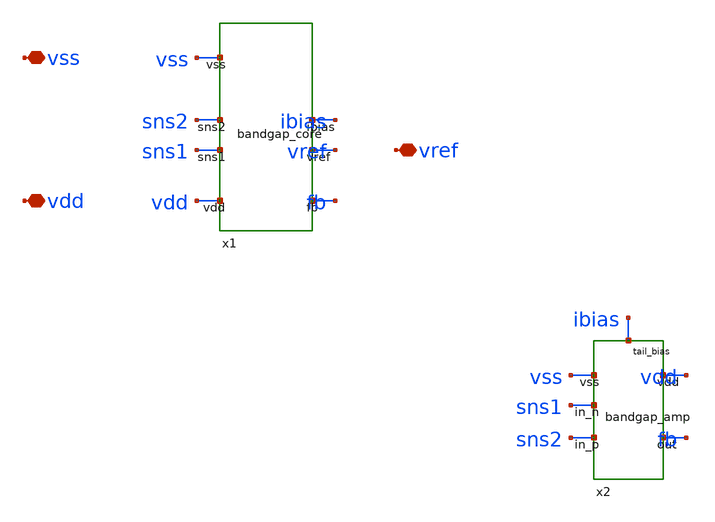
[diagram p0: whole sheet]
** sch_path: design/bandgap_top.sch
**.subckt bandgap_top vdd vss vref
*.iopin vdd
*.iopin vss
*.iopin vref
Xx1 vdd sns1 sns2 vss fb vref ibias bandgap_core
Xx2 sns2 sns1 vss fb vdd ibias bandgap_amp
**.ends

* expanding   symbol:  bandgap_core.sym # of pins=7
** sym_path: design/bandgap_core.sym
** sch_path: design/bandgap_core.sch
.subckt bandgap_core vdd sns1 sns2 vss fb vref ibias

*.iopin vdd
*.iopin vss
*.iopin fb
*.iopin sns1
*.iopin sns2
*.iopin vref
*.iopin ibias
XM1 sns1 fb vdd vdd pfet_03v3 L=2u W=20u nf=1 ad='int((nf+1)/2) * W/nf * 0.18u' as='int((nf+2)/2) * W/nf * 0.18u'
+ pd='2*int((nf+1)/2) * (W/nf + 0.18u)' ps='2*int((nf+2)/2) * (W/nf + 0.18u)' nrd='0.18u / W' nrs='0.18u / W'
+ sa=0 sb=0 sd=0 m=1
XQ1 vss vss sns1 pnp_05p00x05p00 m=1 par=1
XM2 sns2 fb vdd vdd pfet_03v3 L=2u W=20u nf=1 ad='int((nf+1)/2) * W/nf * 0.18u' as='int((nf+2)/2) * W/nf * 0.18u'
+ pd='2*int((nf+1)/2) * (W/nf + 0.18u)' ps='2*int((nf+2)/2) * (W/nf + 0.18u)' nrd='0.18u / W' nrs='0.18u / W'
+ sa=0 sb=0 sd=0 m=1
XR2 e2 sns2 vss ppolyf_u r_width=2u r_length=18u m=1
XQ2 vss vss e2 pnp_10p00x10p00 m=1
XM3 vref fb vdd vdd pfet_03v3 L=2u W=20u nf=1 ad='int((nf+1)/2) * W/nf * 0.18u' as='int((nf+2)/2) * W/nf * 0.18u'
+ pd='2*int((nf+1)/2) * (W/nf + 0.18u)' ps='2*int((nf+2)/2) * (W/nf + 0.18u)' nrd='0.18u / W' nrs='0.18u / W'
+ sa=0 sb=0 sd=0 m=1
XR1 e3 vref vss ppolyf_u r_width=2u r_length=280u m=1
XQ3 vss vss e3 pnp_05p00x05p00 m=1 par=1
XM4 ibias fb vdd vdd pfet_03v3 L=2u W=20u nf=1 ad='int((nf+1)/2) * W/nf * 0.18u' as='int((nf+2)/2) * W/nf * 0.18u'
+ pd='2*int((nf+1)/2) * (W/nf + 0.18u)' ps='2*int((nf+2)/2) * (W/nf + 0.18u)' nrd='0.18u / W' nrs='0.18u / W'
+ sa=0 sb=0 sd=0 m=1
XM5 ibias ibias vss vss nfet_03v3 L=2u W=20u nf=1 ad='int((nf+1)/2) * W/nf * 0.18u' as='int((nf+2)/2) * W/nf * 0.18u'
+ pd='2*int((nf+1)/2) * (W/nf + 0.18u)' ps='2*int((nf+2)/2) * (W/nf + 0.18u)' nrd='0.18u / W' nrs='0.18u / W'
+ sa=0 sb=0 sd=0 m=1
.ends


* expanding   symbol:  bandgap_amp.sym # of pins=6
** sym_path: design/bandgap_amp.sym
** sch_path: design/bandgap_amp.sch
.subckt bandgap_amp in_p in_n vss out vdd tail_bias

*.iopin vdd
*.iopin vss
*.iopin in_p
*.iopin in_n
*.iopin out
*.iopin tail_bias
XM1 nd1 in_p tail vss nfet_03v3 L=4u W=10u nf=1 ad='int((nf+1)/2) * W/nf * 0.18u' as='int((nf+2)/2) * W/nf * 0.18u'
+ pd='2*int((nf+1)/2) * (W/nf + 0.18u)' ps='2*int((nf+2)/2) * (W/nf + 0.18u)' nrd='0.18u / W' nrs='0.18u / W'
+ sa=0 sb=0 sd=0 m=1
XM2 out in_n tail vss nfet_03v3 L=4u W=10u nf=1 ad='int((nf+1)/2) * W/nf * 0.18u' as='int((nf+2)/2) * W/nf * 0.18u'
+ pd='2*int((nf+1)/2) * (W/nf + 0.18u)' ps='2*int((nf+2)/2) * (W/nf + 0.18u)' nrd='0.18u / W' nrs='0.18u / W'
+ sa=0 sb=0 sd=0 m=1
XM3 nd1 nd1 vdd vdd pfet_03v3 L=4u W=10u nf=1 ad='int((nf+1)/2) * W/nf * 0.18u' as='int((nf+2)/2) * W/nf * 0.18u'
+ pd='2*int((nf+1)/2) * (W/nf + 0.18u)' ps='2*int((nf+2)/2) * (W/nf + 0.18u)' nrd='0.18u / W' nrs='0.18u / W'
+ sa=0 sb=0 sd=0 m=1
XM4 out nd1 vdd vdd pfet_03v3 L=4u W=10u nf=1 ad='int((nf+1)/2) * W/nf * 0.18u' as='int((nf+2)/2) * W/nf * 0.18u'
+ pd='2*int((nf+1)/2) * (W/nf + 0.18u)' ps='2*int((nf+2)/2) * (W/nf + 0.18u)' nrd='0.18u / W' nrs='0.18u / W'
+ sa=0 sb=0 sd=0 m=1
XM5 tail tail_bias vss vss nfet_03v3 L=4u W=10u nf=1 ad='int((nf+1)/2) * W/nf * 0.18u' as='int((nf+2)/2) * W/nf * 0.18u'
+ pd='2*int((nf+1)/2) * (W/nf + 0.18u)' ps='2*int((nf+2)/2) * (W/nf + 0.18u)' nrd='0.18u / W' nrs='0.18u / W'
+ sa=0 sb=0 sd=0 m=1
.ends

.end
